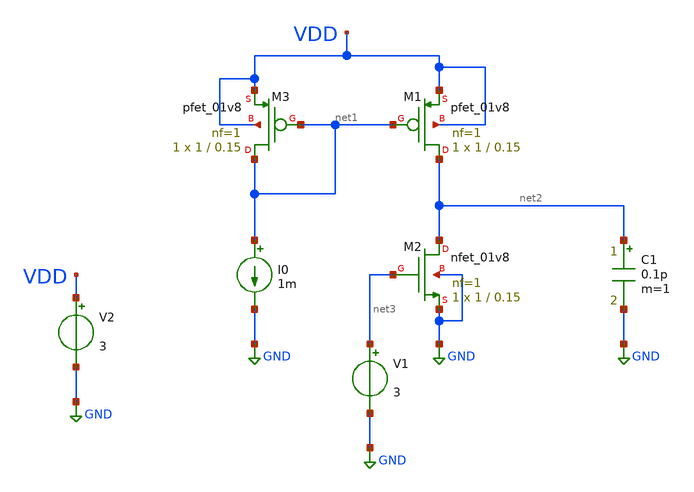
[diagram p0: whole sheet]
** sch_path: otaa.sch
**.subckt otaa
XM2 net2 net3 GND GND sky130_fd_pr__nfet_01v8 L=0.15 W=1 nf=1 ad='int((nf+1)/2) * W/nf * 0.29' as='int((nf+2)/2) * W/nf * 0.29'
+ pd='2*int((nf+1)/2) * (W/nf + 0.29)' ps='2*int((nf+2)/2) * (W/nf + 0.29)' nrd='0.29 / W' nrs='0.29 / W'
+ sa=0 sb=0 sd=0 mult=1 m=1
XM1 net2 net1 VDD VDD sky130_fd_pr__pfet_01v8 L=0.15 W=1 nf=1 ad='int((nf+1)/2) * W/nf * 0.29' as='int((nf+2)/2) * W/nf * 0.29'
+ pd='2*int((nf+1)/2) * (W/nf + 0.29)' ps='2*int((nf+2)/2) * (W/nf + 0.29)' nrd='0.29 / W' nrs='0.29 / W'
+ sa=0 sb=0 sd=0 mult=1 m=1
XM3 net1 net1 VDD VDD sky130_fd_pr__pfet_01v8 L=0.15 W=1 nf=1 ad='int((nf+1)/2) * W/nf * 0.29' as='int((nf+2)/2) * W/nf * 0.29'
+ pd='2*int((nf+1)/2) * (W/nf + 0.29)' ps='2*int((nf+2)/2) * (W/nf + 0.29)' nrd='0.29 / W' nrs='0.29 / W'
+ sa=0 sb=0 sd=0 mult=1 m=1
I0 net1 GND 1m
V1 net3 GND 3
V2 VDD GND 3
C1 net2 GND 0.1p m=1
**.ends
.GLOBAL GND
.end
